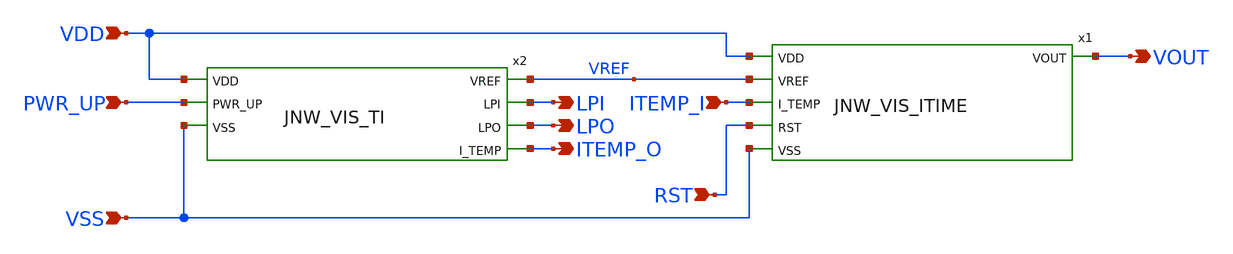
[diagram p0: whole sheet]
** sch_path: design/JNW_GR02_SKY130A/TB_JNW_VIS_ITIME.sch
**.subckt TB_JNW_VIS_ITIME VDD VSS PWR_UP RST VOUT LPI LPO ITEMP_O ITEMP_I
*.ipin VDD
*.ipin VSS
*.ipin PWR_UP
*.ipin RST
*.opin VOUT
*.opin LPI
*.opin LPO
*.opin ITEMP_O
*.ipin ITEMP_I
x1 VDD VREF VOUT ITEMP_I RST VSS JNW_VIS_ITIME
x2 VDD VREF LPI LPO ITEMP_O PWR_UP VSS JNW_VIS_TI
**.ends
.end
